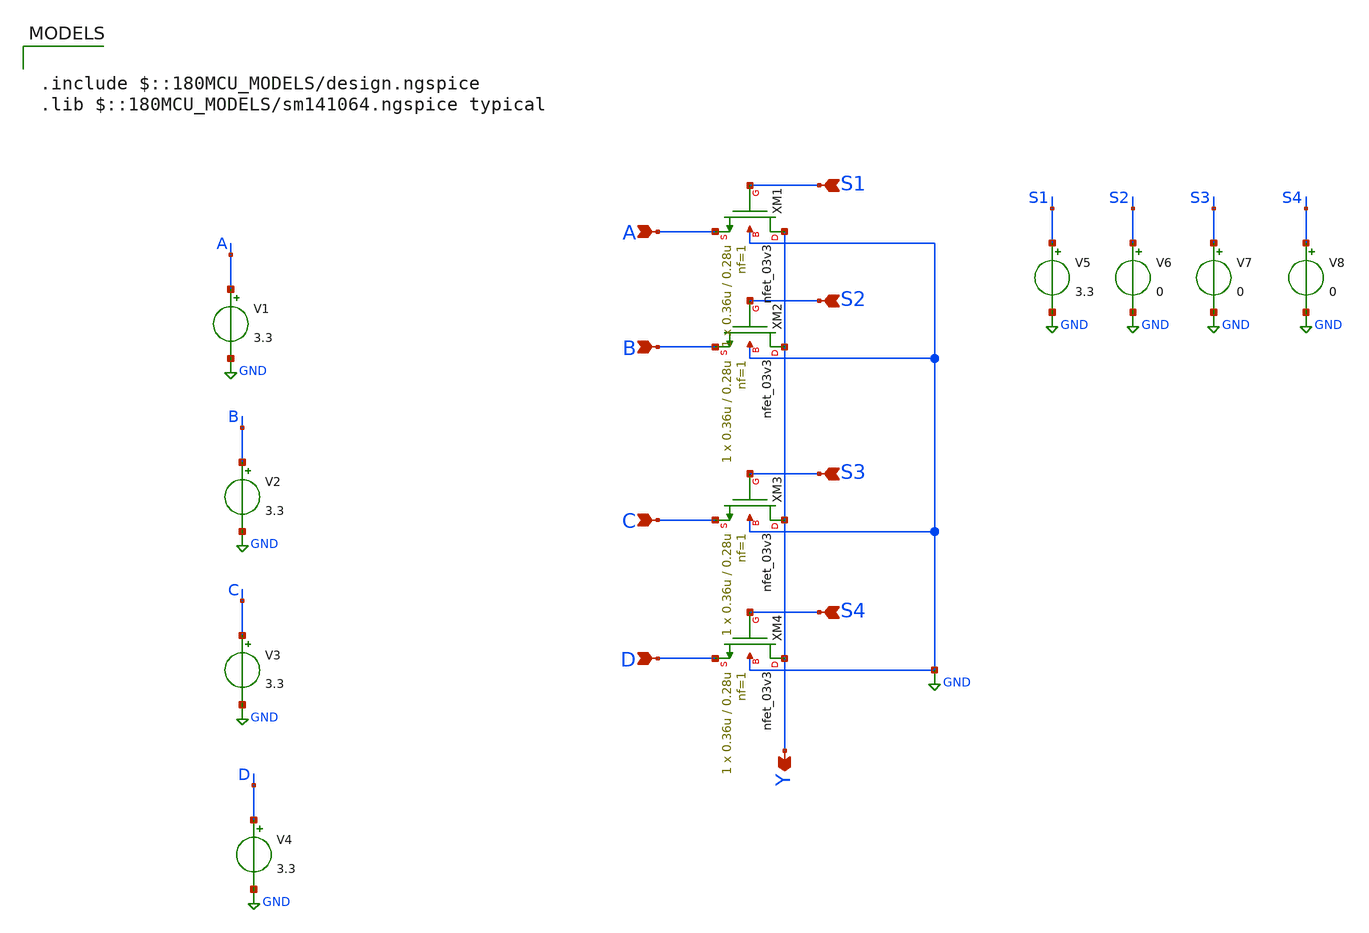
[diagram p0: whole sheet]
** sch_path: CAD4/4_pass_transisors.sch
**.subckt 4_pass_transisors A B C D Y S1 S2 S3 S4
*.ipin A
*.ipin B
*.ipin C
*.ipin D
*.opin Y
*.ipin S1
*.ipin S2
*.ipin S3
*.ipin S4
XM1 Y S1 A GND nfet_03v3 L=0.28u W=0.36u nf=1 ad='int((nf+1)/2) * W/nf * 0.18u' as='int((nf+2)/2) * W/nf * 0.18u'
+ pd='2*int((nf+1)/2) * (W/nf + 0.18u)' ps='2*int((nf+2)/2) * (W/nf + 0.18u)' nrd='0.18u / W' nrs='0.18u / W'
+ sa=0 sb=0 sd=0 m=1
XM2 Y S2 B GND nfet_03v3 L=0.28u W=0.36u nf=1 ad='int((nf+1)/2) * W/nf * 0.18u' as='int((nf+2)/2) * W/nf * 0.18u'
+ pd='2*int((nf+1)/2) * (W/nf + 0.18u)' ps='2*int((nf+2)/2) * (W/nf + 0.18u)' nrd='0.18u / W' nrs='0.18u / W'
+ sa=0 sb=0 sd=0 m=1
XM3 Y S3 C GND nfet_03v3 L=0.28u W=0.36u nf=1 ad='int((nf+1)/2) * W/nf * 0.18u' as='int((nf+2)/2) * W/nf * 0.18u'
+ pd='2*int((nf+1)/2) * (W/nf + 0.18u)' ps='2*int((nf+2)/2) * (W/nf + 0.18u)' nrd='0.18u / W' nrs='0.18u / W'
+ sa=0 sb=0 sd=0 m=1
XM4 Y S4 D GND nfet_03v3 L=0.28u W=0.36u nf=1 ad='int((nf+1)/2) * W/nf * 0.18u' as='int((nf+2)/2) * W/nf * 0.18u'
+ pd='2*int((nf+1)/2) * (W/nf + 0.18u)' ps='2*int((nf+2)/2) * (W/nf + 0.18u)' nrd='0.18u / W' nrs='0.18u / W'
+ sa=0 sb=0 sd=0 m=1
V1 A GND 3.3
V2 B GND 3.3
V3 C GND 3.3
V4 D GND 3.3
V5 S1 GND 3.3
V6 S2 GND 0
V7 S3 GND 0
V8 S4 GND 0
**** begin user architecture code

.include $::180MCU_MODELS/design.ngspice
.lib $::180MCU_MODELS/sm141064.ngspice typical



.control

** timing
let f = 1e8
let T = 1/f
let PW = T/2

let tstop = 4*T
let tstep = 0.001*T

** inputs (A B C D)
alter @V1[PULSE] = [ 0 3.3 0     1n 1n $&PW $&T ]
alter @V2[PULSE] = [ 0 3.3 $&PW  1n 1n $&PW $&T ]
alter @V3[PULSE] = [ 0 3.3 0     1n 1n $&PW $&(2*T) ]
alter @V4[PULSE] = [ 0 3.3 $&PW  1n 1n $&PW $&(2*T) ]

** select lines (one hot encoding)
alter @V5[PWL] = [ 0 3.3 $&T 3.3 $&T 0 ]
alter @V6[PWL] = 0
alter @V7[PWL] = 0
alter @V8[PWL] = 0

** simulation
tran $&tstep $&tstop

** plot
**plot A B+4 C+8 D+12 Y+16
plot A B+4 C+8 D+12 S1+16 Y+32

.endc




**** end user architecture code
**.ends
.GLOBAL GND
.end
